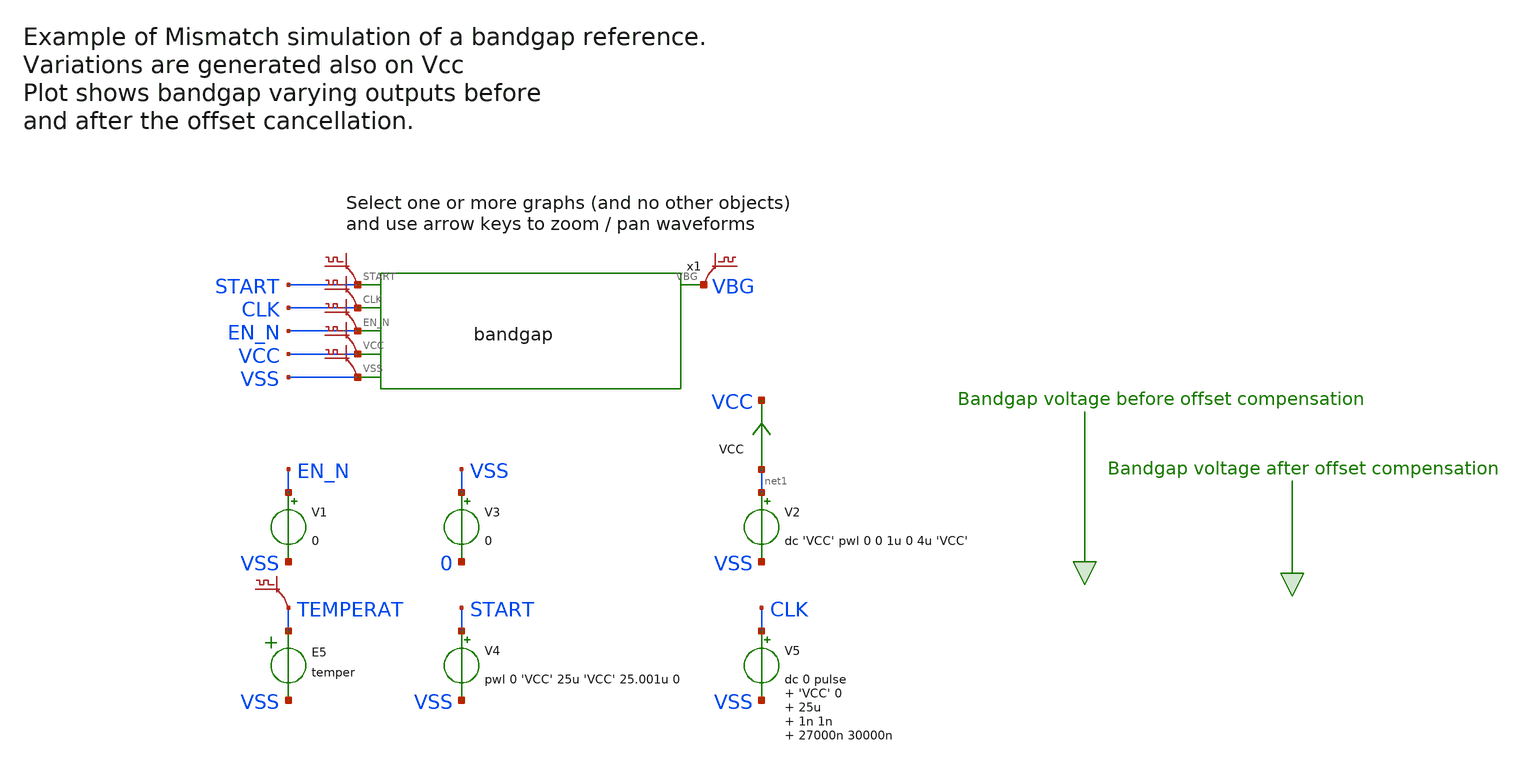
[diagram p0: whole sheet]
** sch_path: sky130A/xschem_libs/sky130_tests_ase/tb_bandgap/schematic/tb_bandgap.sch
* Copyright 2021 Stefan Frederik Schippers
* Licensed under the Apache License, Version 2.0 (the "License");
* you may not use this file except in compliance with the License.
* You may obtain a copy of the License at
* https://www.apache.org/licenses/LICENSE-2.0
* Unless required by applicable law or agreed to in writing, software
* distributed under the License is distributed on an "AS IS" BASIS,
* WITHOUT WARRANTIES OR CONDITIONS OF ANY KIND, either express or implied.
* See the License for the specific language governing permissions and
* limitations under the License.
**.subckt tb_bandgap
x1 START CLK EN_N VBG VCC VSS bandgap
V1 EN_N VSS 0
V2 net1 VSS dc 'VCC' pwl 0 0 1u 0 4u 'VCC'
V3 VSS 0 0
E5 TEMPERAT VSS VOL=' temper '
V4 START VSS pwl 0 'VCC' 25u 'VCC' 25.001u 0
V5 CLK VSS dc 0 pulse 'VCC' 0 25u 1n 1n 27000n 30000n
.save v(vbg)
.save v(start)
.save v(clk)
.save v(en_n)
.save v(vcc)
.save v(vss)
.save v(temperat)
VCC net1 VCC 0
.save i(vcc)
**.ends
.end
